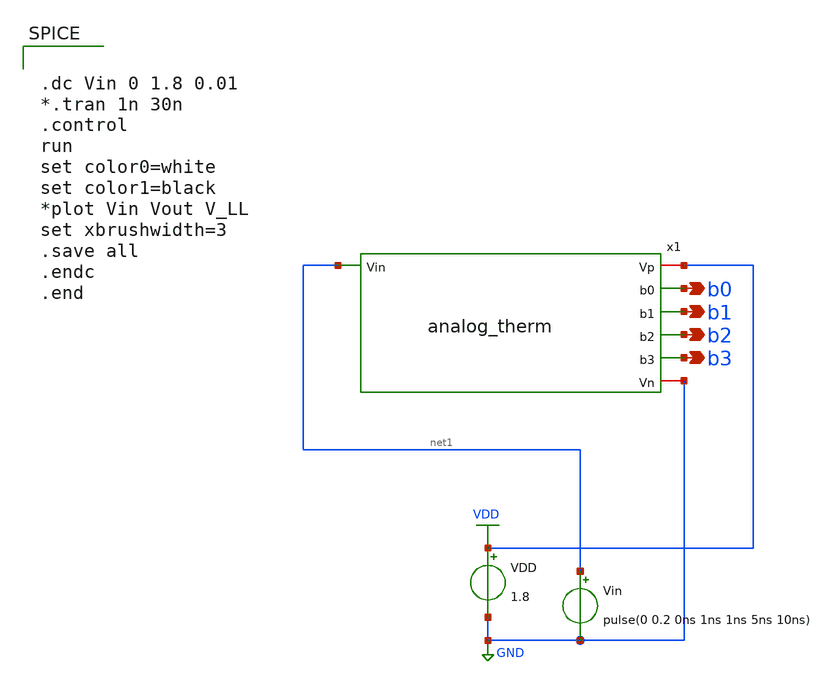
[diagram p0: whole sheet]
** sch_path: xschem/Vth_sch/Pre_layout/Analog_with_sub.sch
**.subckt Analog_with_sub b0 b1 b2 b3
*.opin b0
*.opin b1
*.opin b2
*.opin b3
VDD VDD GND 1.8
Vin net1 GND pulse(0 0.2 0ns 1ns 1ns 5ns 10ns)
x1 VDD net1 b0 b1 b2 b3 GND analog_therm
**** begin user architecture code


.lib /usr/local/share/pdk/sky130A/libs.tech/ngspice/sky130.lib.spice tt
.include /usr/local/share/pdk/sky130A/libs.ref/sky130_fd_sc_hd/spice/sky130_fd_sc_hd.spice
.save all





.dc Vin 0 1.8 0.01
*.tran 1n 30n
.control
run
set color0=white
set color1=black
*plot Vin Vout V_LL
set xbrushwidth=3
.save all
.endc
.end


**** end user architecture code
**.ends

* expanding   symbol:  analog_therm.sym # of pins=7
** sym_path: xschem/Vth_sch/Symbol/analog_therm.sym
** sch_path: xschem/Vth_sch/Symbol/analog_therm.sch
.subckt analog_therm Vp Vin b0 b1 b2 b3 Vn
*.opin b0
*.ipin Vin
*.opin b1
*.opin b2
*.opin b3
*.iopin Vp
*.iopin Vn
x1 p1 p0 VGND VNB VPB VPWR 2 sky130_fd_sc_hd__nand2_1
x2 p1 p0 p2 VGND VNB VPB VPWR 3 sky130_fd_sc_hd__nand3_1
x3 p1 p0 p3 p2 VGND VNB VPB VPWR 4 sky130_fd_sc_hd__nand4_1
x4 p5 p4 VGND VNB VPB VPWR 5 sky130_fd_sc_hd__nand2_1
x5 p5 p4 p7 p6 VGND VNB VPB VPWR 6 sky130_fd_sc_hd__nand4_1
x6 4 6 VGND VNB VPB VPWR 7 sky130_fd_sc_hd__nor2_1
x7 p8 p9 VGND VNB VPB VPWR 8 sky130_fd_sc_hd__nand2_1
x8 p11 p10 VGND VNB VPB VPWR 9 sky130_fd_sc_hd__nand2_1
x9 4 6 8 9 VGND VNB VPB VPWR 10 sky130_fd_sc_hd__nor4_1
x10 p13 p12 VGND VNB VPB VPWR 11 sky130_fd_sc_hd__and2_0
x11 10 11 VGND VNB VPB VPWR 12 sky130_fd_sc_hd__nand2_1
x12 p14 10 11 VGND VNB VPB VPWR 13 sky130_fd_sc_hd__nand3_1
x13 p7 5 VGND VNB VPB VPWR 14 sky130_fd_sc_hd__nor2_1
x14 p5 p7 p6 VGND VNB VPB VPWR 15 sky130_fd_sc_hd__nor3_1
x15 p6 14 15 p4 VGND VNB VPB VPWR 16 sky130_fd_sc_hd__a22oi_1
x16 p13 p14 VGND VNB VPB VPWR 17 sky130_fd_sc_hd__nor2_1
x17 p13 p12 p14 VGND VNB VPB VPWR 18 sky130_fd_sc_hd__or3_1
x18 p11 p10 VGND VNB VPB VPWR 19 sky130_fd_sc_hd__lpflow_inputiso1p_1
x19 p8 p9 18 19 VGND VNB VPB VPWR 20 sky130_fd_sc_hd__nor4_1
x20 4 20 VGND VNB VPB VPWR 21 sky130_fd_sc_hd__nand2b_1
x21 p9 18 19 p8 VGND VNB VPB VPWR 22 sky130_fd_sc_hd__nor4b_1
x22 p11 8 18 VGND VNB VPB VPWR 23 sky130_fd_sc_hd__nor3_1
x23 p11 1 8 18 VGND VNB VPB VPWR 24 sky130_fd_sc_hd__nor4_1
x24 22 24 7 VGND VNB VPB VPWR 25 sky130_fd_sc_hd__o21ai_0
x25 p1 p2 p0 VGND VNB VPB VPWR 26 sky130_fd_sc_hd__or3b_1
x26 p5 p4 p7 p6 VGND VNB VPB VPWR 27 sky130_fd_sc_hd__or4_1
x27 3 26 27 p3 VGND VNB VPB VPWR 28 sky130_fd_sc_hd__a211oi_1
x28 p12 10 17 20 28 VGND VNB VPB VPWR 29 sky130_fd_sc_hd__a32oi_1
x29 16 21 25 29 13 VGND VNB VPB VPWR b0 sky130_fd_sc_hd__o2111ai_1
x30 4 14 20 VGND VNB VPB VPWR 30 sky130_fd_sc_hd__nand3b_1
x31 7 23 VGND VNB VPB VPWR 31 sky130_fd_sc_hd__nand2_1
x32 p3 2 27 VGND VNB VPB VPWR 32 sky130_fd_sc_hd__nor3_1
x33 20 32 VGND VNB VPB VPWR 33 sky130_fd_sc_hd__nand2_1
x34 12 30 31 33 VGND VNB VPB VPWR b1 sky130_fd_sc_hd__nand4_1
x35 11 17 10 VGND VNB VPB VPWR 34 sky130_fd_sc_hd__o21ai_0
x36 14 15 VGND VNB VPB VPWR 35 sky130_fd_sc_hd__nor2_1
x37 21 35 34 VGND VNB VPB VPWR b2 sky130_fd_sc_hd__o21ai_0
x38 20 22 23 7 VGND VNB VPB VPWR 36 sky130_fd_sc_hd__o31ai_1
x39 34 36 VGND VNB VPB VPWR b3 sky130_fd_sc_hd__nand2_1
**** begin user architecture code


vvpwr vpwr 0 dc 1.8
vvgnd vgnd 0 dc 0


**** end user architecture code
x41 p10 VGND VNB VPB VPWR 1 sky130_fd_sc_hd__clkinv_1
x40 Vin Vp p0 p1 p2 p3 p4 p5 p6 p7 p8 p9 p10 p11 p12 p13 p14 Vn Analog
.ends


* expanding   symbol:  Analog.sym # of pins=18
** sym_path: xschem/Vth_sch/Symbol/Analog.sym
** sch_path: xschem/Vth_sch/Symbol/Analog.sch
.subckt Analog Vin Vp V1 V2 V3 V4 V5 V6 V7 V8 V9 V10 V11 V12 V13 V14 V15 Vn
*.ipin Vin
*.opin V1
*.opin V3
*.opin V5
*.opin V7
*.opin V9
*.opin V11
*.opin V13
*.opin V15
*.opin V2
*.opin V4
*.opin V6
*.opin V8
*.opin V10
*.opin V12
*.opin V14
*.iopin Vp
*.iopin Vn
x1 Vp Vin V1 Vn th01
x2 Vp Vin V2 Vn th02
x3 Vp V3 Vin Vn th03
x4 Vp V4 Vin Vn th04
x5 Vp V5 Vin Vn th05
x6 Vp Vin V6 Vn th06
x7 Vp Vin V7 Vn th07
x8 Vp Vin V8 Vn th08
x9 Vp V9 Vin Vn th09
x10 Vp V10 Vin Vn th10
x11 Vp V11 Vin Vn th11
x12 Vp V12 Vin Vn th12
x13 Vp V13 Vin Vn th13
x14 Vp V14 Vin Vn th14
x15 Vp V15 Vin Vn th15
.ends


* expanding   symbol:  Symbol/th01.sym # of pins=4
** sym_path: xschem/Vth_sch/Symbol/th01.sym
** sch_path: xschem/Vth_sch/Symbol/th01.sch
.subckt th01 Vp Vin V01 Vn
*.ipin Vin
*.opin V01
*.iopin Vp
*.iopin Vn
XM3 V01 net1 Vp Vp sky130_fd_pr__pfet_01v8 L=0.15 W=1.5 nf=1 ad='int((nf+1)/2) * W/nf * 0.29' as='int((nf+2)/2) * W/nf * 0.29'
+ pd='2*int((nf+1)/2) * (W/nf + 0.29)' ps='2*int((nf+2)/2) * (W/nf + 0.29)' nrd='0.29 / W' nrs='0.29 / W'
+ sa=0 sb=0 sd=0 mult=1 m=1
XM4 V01 net1 Vn Vn sky130_fd_pr__nfet_01v8 L=1.50 W=0.36 nf=1 ad='int((nf+1)/2) * W/nf * 0.29' as='int((nf+2)/2) * W/nf * 0.29'
+ pd='2*int((nf+1)/2) * (W/nf + 0.29)' ps='2*int((nf+2)/2) * (W/nf + 0.29)' nrd='0.29 / W' nrs='0.29 / W'
+ sa=0 sb=0 sd=0 mult=1 m=1
XM1 net1 Vin net2 Vp sky130_fd_pr__pfet_01v8 L=3.5 W=0.42 nf=1 ad='int((nf+1)/2) * W/nf * 0.29' as='int((nf+2)/2) * W/nf * 0.29'
+ pd='2*int((nf+1)/2) * (W/nf + 0.29)' ps='2*int((nf+2)/2) * (W/nf + 0.29)' nrd='0.29 / W' nrs='0.29 / W'
+ sa=0 sb=0 sd=0 mult=1 m=1
XM0 net1 Vin Vn Vn sky130_fd_pr__nfet_01v8 L=0.15 W=3.525 nf=1 ad='int((nf+1)/2) * W/nf * 0.29' as='int((nf+2)/2) * W/nf * 0.29'
+ pd='2*int((nf+1)/2) * (W/nf + 0.29)' ps='2*int((nf+2)/2) * (W/nf + 0.29)' nrd='0.29 / W' nrs='0.29 / W'
+ sa=0 sb=0 sd=0 mult=1 m=1
XM2 Vp Vp net2 Vn sky130_fd_pr__nfet_01v8 L=3.5 W=0.36 nf=1 ad='int((nf+1)/2) * W/nf * 0.29' as='int((nf+2)/2) * W/nf * 0.29'
+ pd='2*int((nf+1)/2) * (W/nf + 0.29)' ps='2*int((nf+2)/2) * (W/nf + 0.29)' nrd='0.29 / W' nrs='0.29 / W'
+ sa=0 sb=0 sd=0 mult=1 m=1
.ends


* expanding   symbol:  Symbol/th02.sym # of pins=4
** sym_path: xschem/Vth_sch/Symbol/th02.sym
** sch_path: xschem/Vth_sch/Symbol/th02.sch
.subckt th02 Vp Vin V02 Vn
*.ipin Vin
*.opin V02
*.iopin Vp
*.iopin Vn
XM3 V02 net1 Vp Vp sky130_fd_pr__pfet_01v8 L=0.15 W=1.5 nf=1 ad='int((nf+1)/2) * W/nf * 0.29' as='int((nf+2)/2) * W/nf * 0.29'
+ pd='2*int((nf+1)/2) * (W/nf + 0.29)' ps='2*int((nf+2)/2) * (W/nf + 0.29)' nrd='0.29 / W' nrs='0.29 / W'
+ sa=0 sb=0 sd=0 mult=1 m=1
XM4 V02 net1 Vn Vn sky130_fd_pr__nfet_01v8 L=1.50 W=0.36 nf=1 ad='int((nf+1)/2) * W/nf * 0.29' as='int((nf+2)/2) * W/nf * 0.29'
+ pd='2*int((nf+1)/2) * (W/nf + 0.29)' ps='2*int((nf+2)/2) * (W/nf + 0.29)' nrd='0.29 / W' nrs='0.29 / W'
+ sa=0 sb=0 sd=0 mult=1 m=1
XM1 net1 Vin net2 Vp sky130_fd_pr__pfet_01v8 L=1.53 W=0.42 nf=1 ad='int((nf+1)/2) * W/nf * 0.29' as='int((nf+2)/2) * W/nf * 0.29'
+ pd='2*int((nf+1)/2) * (W/nf + 0.29)' ps='2*int((nf+2)/2) * (W/nf + 0.29)' nrd='0.29 / W' nrs='0.29 / W'
+ sa=0 sb=0 sd=0 mult=1 m=1
XM0 net1 Vin Vn Vn sky130_fd_pr__nfet_01v8 L=0.15 W=1.5 nf=2 ad='int((nf+1)/2) * W/nf * 0.29' as='int((nf+2)/2) * W/nf * 0.29'
+ pd='2*int((nf+1)/2) * (W/nf + 0.29)' ps='2*int((nf+2)/2) * (W/nf + 0.29)' nrd='0.29 / W' nrs='0.29 / W'
+ sa=0 sb=0 sd=0 mult=1 m=1
XM2 Vp Vp net2 Vn sky130_fd_pr__nfet_01v8 L=1.54 W=0.36 nf=1 ad='int((nf+1)/2) * W/nf * 0.29' as='int((nf+2)/2) * W/nf * 0.29'
+ pd='2*int((nf+1)/2) * (W/nf + 0.29)' ps='2*int((nf+2)/2) * (W/nf + 0.29)' nrd='0.29 / W' nrs='0.29 / W'
+ sa=0 sb=0 sd=0 mult=1 m=1
.ends


* expanding   symbol:  Symbol/th03.sym # of pins=4
** sym_path: xschem/Vth_sch/Symbol/th03.sym
** sch_path: xschem/Vth_sch/Symbol/th03.sch
.subckt th03 Vp V03 Vin Vn
*.opin Vn
*.opin Vp
*.ipin Vin
*.opin V03
XM3 V03 net1 Vp Vp sky130_fd_pr__pfet_01v8 L=0.156 W=1.0 nf=1 ad='int((nf+1)/2) * W/nf * 0.29' as='int((nf+2)/2) * W/nf * 0.29'
+ pd='2*int((nf+1)/2) * (W/nf + 0.29)' ps='2*int((nf+2)/2) * (W/nf + 0.29)' nrd='0.29 / W' nrs='0.29 / W'
+ sa=0 sb=0 sd=0 mult=1 m=1
XM4 V03 net1 Vn Vn sky130_fd_pr__nfet_01v8 L=1.5 W=0.40 nf=1 ad='int((nf+1)/2) * W/nf * 0.29' as='int((nf+2)/2) * W/nf * 0.29'
+ pd='2*int((nf+1)/2) * (W/nf + 0.29)' ps='2*int((nf+2)/2) * (W/nf + 0.29)' nrd='0.29 / W' nrs='0.29 / W'
+ sa=0 sb=0 sd=0 mult=1 m=1
XM1 net1 Vin net2 Vp sky130_fd_pr__pfet_01v8 L=1.36 W=0.44 nf=1 ad='int((nf+1)/2) * W/nf * 0.29' as='int((nf+2)/2) * W/nf * 0.29'
+ pd='2*int((nf+1)/2) * (W/nf + 0.29)' ps='2*int((nf+2)/2) * (W/nf + 0.29)' nrd='0.29 / W' nrs='0.29 / W'
+ sa=0 sb=0 sd=0 mult=1 m=1
XM0 net1 Vin Vn Vn sky130_fd_pr__nfet_01v8 L=0.153 W=1.1 nf=1 ad='int((nf+1)/2) * W/nf * 0.29' as='int((nf+2)/2) * W/nf * 0.29'
+ pd='2*int((nf+1)/2) * (W/nf + 0.29)' ps='2*int((nf+2)/2) * (W/nf + 0.29)' nrd='0.29 / W' nrs='0.29 / W'
+ sa=0 sb=0 sd=0 mult=1 m=1
XM2 Vp Vp net2 Vn sky130_fd_pr__nfet_01v8 L=1.5 W=0.36 nf=1 ad='int((nf+1)/2) * W/nf * 0.29' as='int((nf+2)/2) * W/nf * 0.29'
+ pd='2*int((nf+1)/2) * (W/nf + 0.29)' ps='2*int((nf+2)/2) * (W/nf + 0.29)' nrd='0.29 / W' nrs='0.29 / W'
+ sa=0 sb=0 sd=0 mult=1 m=1
.ends


* expanding   symbol:  Symbol/th04.sym # of pins=4
** sym_path: xschem/Vth_sch/Symbol/th04.sym
** sch_path: xschem/Vth_sch/Symbol/th04.sch
.subckt th04 Vp V04 Vin Vn
*.opin Vn
*.opin Vp
*.ipin Vin
*.opin V04
XM3 V04 net1 Vp Vp sky130_fd_pr__pfet_01v8 L=0.220 W=0.42 nf=1 ad='int((nf+1)/2) * W/nf * 0.29' as='int((nf+2)/2) * W/nf * 0.29'
+ pd='2*int((nf+1)/2) * (W/nf + 0.29)' ps='2*int((nf+2)/2) * (W/nf + 0.29)' nrd='0.29 / W' nrs='0.29 / W'
+ sa=0 sb=0 sd=0 mult=1 m=1
XM4 V04 net1 Vn Vn sky130_fd_pr__nfet_01v8 L=0.193 W=0.36 nf=1 ad='int((nf+1)/2) * W/nf * 0.29' as='int((nf+2)/2) * W/nf * 0.29'
+ pd='2*int((nf+1)/2) * (W/nf + 0.29)' ps='2*int((nf+2)/2) * (W/nf + 0.29)' nrd='0.29 / W' nrs='0.29 / W'
+ sa=0 sb=0 sd=0 mult=1 m=1
XM1 net1 Vin net2 Vp sky130_fd_pr__pfet_01v8 L=0.193 W=0.42 nf=1 ad='int((nf+1)/2) * W/nf * 0.29' as='int((nf+2)/2) * W/nf * 0.29'
+ pd='2*int((nf+1)/2) * (W/nf + 0.29)' ps='2*int((nf+2)/2) * (W/nf + 0.29)' nrd='0.29 / W' nrs='0.29 / W'
+ sa=0 sb=0 sd=0 mult=1 m=1
XM0 net1 Vin Vn Vn sky130_fd_pr__nfet_01v8 L=0.220 W=0.36 nf=1 ad='int((nf+1)/2) * W/nf * 0.29' as='int((nf+2)/2) * W/nf * 0.29'
+ pd='2*int((nf+1)/2) * (W/nf + 0.29)' ps='2*int((nf+2)/2) * (W/nf + 0.29)' nrd='0.29 / W' nrs='0.29 / W'
+ sa=0 sb=0 sd=0 mult=1 m=1
XM2 Vp Vp net2 Vn sky130_fd_pr__nfet_01v8 L=0.151 W=0.36 nf=1 ad='int((nf+1)/2) * W/nf * 0.29' as='int((nf+2)/2) * W/nf * 0.29'
+ pd='2*int((nf+1)/2) * (W/nf + 0.29)' ps='2*int((nf+2)/2) * (W/nf + 0.29)' nrd='0.29 / W' nrs='0.29 / W'
+ sa=0 sb=0 sd=0 mult=1 m=1
.ends


* expanding   symbol:  Symbol/th05.sym # of pins=4
** sym_path: xschem/Vth_sch/Symbol/th05.sym
** sch_path: xschem/Vth_sch/Symbol/th05.sch
.subckt th05 Vp V05 Vin Vn
*.opin Vn
*.opin Vp
*.ipin Vin
*.opin V05
XM2 V05 net1 Vp Vp sky130_fd_pr__pfet_01v8 L=1.12 W=0.5 nf=1 ad='int((nf+1)/2) * W/nf * 0.29' as='int((nf+2)/2) * W/nf * 0.29'
+ pd='2*int((nf+1)/2) * (W/nf + 0.29)' ps='2*int((nf+2)/2) * (W/nf + 0.29)' nrd='0.29 / W' nrs='0.29 / W'
+ sa=0 sb=0 sd=0 mult=1 m=1
XM3 V05 net1 Vn Vn sky130_fd_pr__nfet_01v8 L=0.18 W=1.0 nf=1 ad='int((nf+1)/2) * W/nf * 0.29' as='int((nf+2)/2) * W/nf * 0.29'
+ pd='2*int((nf+1)/2) * (W/nf + 0.29)' ps='2*int((nf+2)/2) * (W/nf + 0.29)' nrd='0.29 / W' nrs='0.29 / W'
+ sa=0 sb=0 sd=0 mult=1 m=1
XM1 net1 Vin Vp Vp sky130_fd_pr__pfet_01v8 L=1.633 W=0.42 nf=1 ad='int((nf+1)/2) * W/nf * 0.29' as='int((nf+2)/2) * W/nf * 0.29'
+ pd='2*int((nf+1)/2) * (W/nf + 0.29)' ps='2*int((nf+2)/2) * (W/nf + 0.29)' nrd='0.29 / W' nrs='0.29 / W'
+ sa=0 sb=0 sd=0 mult=1 m=1
XM0 net1 Vin Vn Vn sky130_fd_pr__nfet_01v8 L=0.2 W=2.00 nf=1 ad='int((nf+1)/2) * W/nf * 0.29' as='int((nf+2)/2) * W/nf * 0.29'
+ pd='2*int((nf+1)/2) * (W/nf + 0.29)' ps='2*int((nf+2)/2) * (W/nf + 0.29)' nrd='0.29 / W' nrs='0.29 / W'
+ sa=0 sb=0 sd=0 mult=1 m=1
.ends


* expanding   symbol:  Symbol/th06.sym # of pins=4
** sym_path: xschem/Vth_sch/Symbol/th06.sym
** sch_path: xschem/Vth_sch/Symbol/th06.sch
.subckt th06 Vp Vin V06 Vn
*.opin Vn
*.opin Vp
*.ipin Vin
*.opin V06
XM2 V06 net1 Vp Vp sky130_fd_pr__pfet_01v8 L=0.436 W=0.422 nf=1 ad='int((nf+1)/2) * W/nf * 0.29' as='int((nf+2)/2) * W/nf * 0.29'
+ pd='2*int((nf+1)/2) * (W/nf + 0.29)' ps='2*int((nf+2)/2) * (W/nf + 0.29)' nrd='0.29 / W' nrs='0.29 / W'
+ sa=0 sb=0 sd=0 mult=1 m=1
XM3 V06 net1 Vn Vn sky130_fd_pr__nfet_01v8 L=0.15 W=0.462 nf=1 ad='int((nf+1)/2) * W/nf * 0.29' as='int((nf+2)/2) * W/nf * 0.29'
+ pd='2*int((nf+1)/2) * (W/nf + 0.29)' ps='2*int((nf+2)/2) * (W/nf + 0.29)' nrd='0.29 / W' nrs='0.29 / W'
+ sa=0 sb=0 sd=0 mult=1 m=1
XM1 net1 Vin Vp Vp sky130_fd_pr__pfet_01v8 L=0.494 W=0.42 nf=1 ad='int((nf+1)/2) * W/nf * 0.29' as='int((nf+2)/2) * W/nf * 0.29'
+ pd='2*int((nf+1)/2) * (W/nf + 0.29)' ps='2*int((nf+2)/2) * (W/nf + 0.29)' nrd='0.29 / W' nrs='0.29 / W'
+ sa=0 sb=0 sd=0 mult=1 m=1
XM0 net1 Vin Vn Vn sky130_fd_pr__nfet_01v8 L=0.152 W=0.393 nf=1 ad='int((nf+1)/2) * W/nf * 0.29' as='int((nf+2)/2) * W/nf * 0.29'
+ pd='2*int((nf+1)/2) * (W/nf + 0.29)' ps='2*int((nf+2)/2) * (W/nf + 0.29)' nrd='0.29 / W' nrs='0.29 / W'
+ sa=0 sb=0 sd=0 mult=1 m=1
.ends


* expanding   symbol:  Symbol/th07.sym # of pins=4
** sym_path: xschem/Vth_sch/Symbol/th07.sym
** sch_path: xschem/Vth_sch/Symbol/th07.sch
.subckt th07 Vp Vin V07 Vn
*.opin Vn
*.opin Vp
*.ipin Vin
*.opin V07
XM2 V07 net1 Vp Vp sky130_fd_pr__pfet_01v8 L=0.5 W=0.42 nf=1 ad='int((nf+1)/2) * W/nf * 0.29' as='int((nf+2)/2) * W/nf * 0.29'
+ pd='2*int((nf+1)/2) * (W/nf + 0.29)' ps='2*int((nf+2)/2) * (W/nf + 0.29)' nrd='0.29 / W' nrs='0.29 / W'
+ sa=0 sb=0 sd=0 mult=1 m=1
XM3 V07 net1 Vn Vn sky130_fd_pr__nfet_01v8 L=0.15 W=0.462 nf=1 ad='int((nf+1)/2) * W/nf * 0.29' as='int((nf+2)/2) * W/nf * 0.29'
+ pd='2*int((nf+1)/2) * (W/nf + 0.29)' ps='2*int((nf+2)/2) * (W/nf + 0.29)' nrd='0.29 / W' nrs='0.29 / W'
+ sa=0 sb=0 sd=0 mult=1 m=1
XM1 net1 Vin Vp Vp sky130_fd_pr__pfet_01v8 L=0.151 W=0.42 nf=1 ad='int((nf+1)/2) * W/nf * 0.29' as='int((nf+2)/2) * W/nf * 0.29'
+ pd='2*int((nf+1)/2) * (W/nf + 0.29)' ps='2*int((nf+2)/2) * (W/nf + 0.29)' nrd='0.29 / W' nrs='0.29 / W'
+ sa=0 sb=0 sd=0 mult=1 m=1
XM0 net1 Vin Vn Vn sky130_fd_pr__nfet_01v8 L=0.155 W=0.36 nf=1 ad='int((nf+1)/2) * W/nf * 0.29' as='int((nf+2)/2) * W/nf * 0.29'
+ pd='2*int((nf+1)/2) * (W/nf + 0.29)' ps='2*int((nf+2)/2) * (W/nf + 0.29)' nrd='0.29 / W' nrs='0.29 / W'
+ sa=0 sb=0 sd=0 mult=1 m=1
.ends


* expanding   symbol:  Symbol/th08.sym # of pins=4
** sym_path: xschem/Vth_sch/Symbol/th08.sym
** sch_path: xschem/Vth_sch/Symbol/th08.sch
.subckt th08 Vp Vin V08 Vn
*.opin Vn
*.opin Vp
*.ipin Vin
*.opin V08
XM2 V08 net1 Vp Vp sky130_fd_pr__pfet_01v8 L=0.48 W=0.43 nf=1 ad='int((nf+1)/2) * W/nf * 0.29' as='int((nf+2)/2) * W/nf * 0.29'
+ pd='2*int((nf+1)/2) * (W/nf + 0.29)' ps='2*int((nf+2)/2) * (W/nf + 0.29)' nrd='0.29 / W' nrs='0.29 / W'
+ sa=0 sb=0 sd=0 mult=1 m=1
XM3 V08 net1 Vn Vn sky130_fd_pr__nfet_01v8 L=0.15 W=0.468 nf=1 ad='int((nf+1)/2) * W/nf * 0.29' as='int((nf+2)/2) * W/nf * 0.29'
+ pd='2*int((nf+1)/2) * (W/nf + 0.29)' ps='2*int((nf+2)/2) * (W/nf + 0.29)' nrd='0.29 / W' nrs='0.29 / W'
+ sa=0 sb=0 sd=0 mult=1 m=1
XM1 net1 Vin Vp Vp sky130_fd_pr__pfet_01v8 L=0.16 W=0.668 nf=1 ad='int((nf+1)/2) * W/nf * 0.29' as='int((nf+2)/2) * W/nf * 0.29'
+ pd='2*int((nf+1)/2) * (W/nf + 0.29)' ps='2*int((nf+2)/2) * (W/nf + 0.29)' nrd='0.29 / W' nrs='0.29 / W'
+ sa=0 sb=0 sd=0 mult=1 m=1
XM0 net1 Vin Vn Vn sky130_fd_pr__nfet_01v8 L=1.13 W=0.36 nf=1 ad='int((nf+1)/2) * W/nf * 0.29' as='int((nf+2)/2) * W/nf * 0.29'
+ pd='2*int((nf+1)/2) * (W/nf + 0.29)' ps='2*int((nf+2)/2) * (W/nf + 0.29)' nrd='0.29 / W' nrs='0.29 / W'
+ sa=0 sb=0 sd=0 mult=1 m=1
.ends


* expanding   symbol:  Symbol/th09.sym # of pins=4
** sym_path: xschem/Vth_sch/Symbol/th09.sym
** sch_path: xschem/Vth_sch/Symbol/th09.sch
.subckt th09 Vp V09 Vin Vn
*.ipin Vin
*.opin V09
*.opin Vn
*.opin Vp
XM2 net2 net1 Vp Vp sky130_fd_pr__pfet_01v8 L=1.57 W=0.42 nf=1 ad='int((nf+1)/2) * W/nf * 0.29' as='int((nf+2)/2) * W/nf * 0.29'
+ pd='2*int((nf+1)/2) * (W/nf + 0.29)' ps='2*int((nf+2)/2) * (W/nf + 0.29)' nrd='0.29 / W' nrs='0.29 / W'
+ sa=0 sb=0 sd=0 mult=1 m=1
XM3 V09 net1 net2 Vp sky130_fd_pr__pfet_01v8 L=1.57 W=0.42 nf=1 ad='int((nf+1)/2) * W/nf * 0.29' as='int((nf+2)/2) * W/nf * 0.29'
+ pd='2*int((nf+1)/2) * (W/nf + 0.29)' ps='2*int((nf+2)/2) * (W/nf + 0.29)' nrd='0.29 / W' nrs='0.29 / W'
+ sa=0 sb=0 sd=0 mult=1 m=1
XM4 V09 net1 Vn Vn sky130_fd_pr__nfet_01v8 L=0.15 W=1.57 nf=1 ad='int((nf+1)/2) * W/nf * 0.29' as='int((nf+2)/2) * W/nf * 0.29'
+ pd='2*int((nf+1)/2) * (W/nf + 0.29)' ps='2*int((nf+2)/2) * (W/nf + 0.29)' nrd='0.29 / W' nrs='0.29 / W'
+ sa=0 sb=0 sd=0 mult=1 m=1
XM1 net1 Vin Vp Vp sky130_fd_pr__pfet_01v8 L=0.15 W=1.58 nf=1 ad='int((nf+1)/2) * W/nf * 0.29' as='int((nf+2)/2) * W/nf * 0.29'
+ pd='2*int((nf+1)/2) * (W/nf + 0.29)' ps='2*int((nf+2)/2) * (W/nf + 0.29)' nrd='0.29 / W' nrs='0.29 / W'
+ sa=0 sb=0 sd=0 mult=1 m=1
XM0 net1 Vin Vn Vn sky130_fd_pr__nfet_01v8 L=1.58 W=0.36 nf=1 ad='int((nf+1)/2) * W/nf * 0.29' as='int((nf+2)/2) * W/nf * 0.29'
+ pd='2*int((nf+1)/2) * (W/nf + 0.29)' ps='2*int((nf+2)/2) * (W/nf + 0.29)' nrd='0.29 / W' nrs='0.29 / W'
+ sa=0 sb=0 sd=0 mult=1 m=1
.ends


* expanding   symbol:  Symbol/th10.sym # of pins=4
** sym_path: xschem/Vth_sch/Symbol/th10.sym
** sch_path: xschem/Vth_sch/Symbol/th10.sch
.subckt th10 Vp V10 Vin Vn
*.opin Vn
*.opin Vp
*.ipin Vin
*.opin V10
XM3 V10 net1 Vp Vp sky130_fd_pr__pfet_01v8 L=0.15 W=0.42 nf=1 ad='int((nf+1)/2) * W/nf * 0.29' as='int((nf+2)/2) * W/nf * 0.29'
+ pd='2*int((nf+1)/2) * (W/nf + 0.29)' ps='2*int((nf+2)/2) * (W/nf + 0.29)' nrd='0.29 / W' nrs='0.29 / W'
+ sa=0 sb=0 sd=0 mult=1 m=1
XM4 V10 net1 Vn Vn sky130_fd_pr__nfet_01v8 L=0.18 W=0.42 nf=1 ad='int((nf+1)/2) * W/nf * 0.29' as='int((nf+2)/2) * W/nf * 0.29'
+ pd='2*int((nf+1)/2) * (W/nf + 0.29)' ps='2*int((nf+2)/2) * (W/nf + 0.29)' nrd='0.29 / W' nrs='0.29 / W'
+ sa=0 sb=0 sd=0 mult=1 m=1
XM2 net1 Vin Vp Vp sky130_fd_pr__pfet_01v8 L=0.28 W=0.42 nf=1 ad='int((nf+1)/2) * W/nf * 0.29' as='int((nf+2)/2) * W/nf * 0.29'
+ pd='2*int((nf+1)/2) * (W/nf + 0.29)' ps='2*int((nf+2)/2) * (W/nf + 0.29)' nrd='0.29 / W' nrs='0.29 / W'
+ sa=0 sb=0 sd=0 mult=1 m=1
XM1 net1 Vin net2 Vn sky130_fd_pr__nfet_01v8 L=0.46 W=0.40 nf=1 ad='int((nf+1)/2) * W/nf * 0.29' as='int((nf+2)/2) * W/nf * 0.29'
+ pd='2*int((nf+1)/2) * (W/nf + 0.29)' ps='2*int((nf+2)/2) * (W/nf + 0.29)' nrd='0.29 / W' nrs='0.29 / W'
+ sa=0 sb=0 sd=0 mult=1 m=1
XM0 Vn Vn net2 Vp sky130_fd_pr__pfet_01v8 L=0.15 W=1 nf=1 ad='int((nf+1)/2) * W/nf * 0.29' as='int((nf+2)/2) * W/nf * 0.29'
+ pd='2*int((nf+1)/2) * (W/nf + 0.29)' ps='2*int((nf+2)/2) * (W/nf + 0.29)' nrd='0.29 / W' nrs='0.29 / W'
+ sa=0 sb=0 sd=0 mult=1 m=1
.ends


* expanding   symbol:  Symbol/th11.sym # of pins=4
** sym_path: xschem/Vth_sch/Symbol/th11.sym
** sch_path: xschem/Vth_sch/Symbol/th11.sch
.subckt th11 Vp V11 Vin Vn
*.opin Vn
*.opin Vp
*.ipin Vin
*.opin V11
XM3 V11 net1 Vp Vp sky130_fd_pr__pfet_01v8 L=0.5 W=0.42 nf=1 ad='int((nf+1)/2) * W/nf * 0.29' as='int((nf+2)/2) * W/nf * 0.29'
+ pd='2*int((nf+1)/2) * (W/nf + 0.29)' ps='2*int((nf+2)/2) * (W/nf + 0.29)' nrd='0.29 / W' nrs='0.29 / W'
+ sa=0 sb=0 sd=0 mult=1 m=1
XM4 V11 net1 Vn Vn sky130_fd_pr__nfet_01v8 L=0.15 W=0.5 nf=1 ad='int((nf+1)/2) * W/nf * 0.29' as='int((nf+2)/2) * W/nf * 0.29'
+ pd='2*int((nf+1)/2) * (W/nf + 0.29)' ps='2*int((nf+2)/2) * (W/nf + 0.29)' nrd='0.29 / W' nrs='0.29 / W'
+ sa=0 sb=0 sd=0 mult=1 m=1
XM2 net1 Vin Vp Vp sky130_fd_pr__pfet_01v8 L=0.15 W=0.43 nf=1 ad='int((nf+1)/2) * W/nf * 0.29' as='int((nf+2)/2) * W/nf * 0.29'
+ pd='2*int((nf+1)/2) * (W/nf + 0.29)' ps='2*int((nf+2)/2) * (W/nf + 0.29)' nrd='0.29 / W' nrs='0.29 / W'
+ sa=0 sb=0 sd=0 mult=1 m=1
XM1 net1 Vin net2 Vn sky130_fd_pr__nfet_01v8 L=1.8 W=0.36 nf=1 ad='int((nf+1)/2) * W/nf * 0.29' as='int((nf+2)/2) * W/nf * 0.29'
+ pd='2*int((nf+1)/2) * (W/nf + 0.29)' ps='2*int((nf+2)/2) * (W/nf + 0.29)' nrd='0.29 / W' nrs='0.29 / W'
+ sa=0 sb=0 sd=0 mult=1 m=1
XM0 Vn Vn net2 Vp sky130_fd_pr__pfet_01v8 L=0.15 W=2 nf=1 ad='int((nf+1)/2) * W/nf * 0.29' as='int((nf+2)/2) * W/nf * 0.29'
+ pd='2*int((nf+1)/2) * (W/nf + 0.29)' ps='2*int((nf+2)/2) * (W/nf + 0.29)' nrd='0.29 / W' nrs='0.29 / W'
+ sa=0 sb=0 sd=0 mult=1 m=1
.ends


* expanding   symbol:  Symbol/th12.sym # of pins=4
** sym_path: xschem/Vth_sch/Symbol/th12.sym
** sch_path: xschem/Vth_sch/Symbol/th12.sch
.subckt th12 Vp V12 Vin Vn
*.opin Vn
*.opin Vp
*.ipin Vin
*.opin V12
XM3 V12 net1 Vp Vp sky130_fd_pr__pfet_01v8 L=1.0 W=0.42 nf=1 ad='int((nf+1)/2) * W/nf * 0.29' as='int((nf+2)/2) * W/nf * 0.29'
+ pd='2*int((nf+1)/2) * (W/nf + 0.29)' ps='2*int((nf+2)/2) * (W/nf + 0.29)' nrd='0.29 / W' nrs='0.29 / W'
+ sa=0 sb=0 sd=0 mult=1 m=1
XM4 V12 net1 Vn Vn sky130_fd_pr__nfet_01v8 L=0.15 W=1.0 nf=1 ad='int((nf+1)/2) * W/nf * 0.29' as='int((nf+2)/2) * W/nf * 0.29'
+ pd='2*int((nf+1)/2) * (W/nf + 0.29)' ps='2*int((nf+2)/2) * (W/nf + 0.29)' nrd='0.29 / W' nrs='0.29 / W'
+ sa=0 sb=0 sd=0 mult=1 m=1
XM2 net1 Vin Vp Vp sky130_fd_pr__pfet_01v8 L=0.15 W=1.0 nf=1 ad='int((nf+1)/2) * W/nf * 0.29' as='int((nf+2)/2) * W/nf * 0.29'
+ pd='2*int((nf+1)/2) * (W/nf + 0.29)' ps='2*int((nf+2)/2) * (W/nf + 0.29)' nrd='0.29 / W' nrs='0.29 / W'
+ sa=0 sb=0 sd=0 mult=1 m=1
XM1 net1 Vin net2 Vn sky130_fd_pr__nfet_01v8 L=2.90 W=0.36 nf=1 ad='int((nf+1)/2) * W/nf * 0.29' as='int((nf+2)/2) * W/nf * 0.29'
+ pd='2*int((nf+1)/2) * (W/nf + 0.29)' ps='2*int((nf+2)/2) * (W/nf + 0.29)' nrd='0.29 / W' nrs='0.29 / W'
+ sa=0 sb=0 sd=0 mult=1 m=1
XM0 Vn Vn net2 Vp sky130_fd_pr__pfet_01v8 L=0.151 W=1.349 nf=1 ad='int((nf+1)/2) * W/nf * 0.29' as='int((nf+2)/2) * W/nf * 0.29'
+ pd='2*int((nf+1)/2) * (W/nf + 0.29)' ps='2*int((nf+2)/2) * (W/nf + 0.29)' nrd='0.29 / W' nrs='0.29 / W'
+ sa=0 sb=0 sd=0 mult=1 m=1
.ends


* expanding   symbol:  Symbol/th13.sym # of pins=4
** sym_path: xschem/Vth_sch/Symbol/th13.sym
** sch_path: xschem/Vth_sch/Symbol/th13.sch
.subckt th13 Vp V13 Vin Vn
*.opin Vn
*.opin Vp
*.ipin Vin
*.opin V13
XM3 V13 net1 Vp Vp sky130_fd_pr__pfet_01v8 L=2 W=0.42 nf=1 ad='int((nf+1)/2) * W/nf * 0.29' as='int((nf+2)/2) * W/nf * 0.29'
+ pd='2*int((nf+1)/2) * (W/nf + 0.29)' ps='2*int((nf+2)/2) * (W/nf + 0.29)' nrd='0.29 / W' nrs='0.29 / W'
+ sa=0 sb=0 sd=0 mult=1 m=1
XM4 V13 net1 Vn Vn sky130_fd_pr__nfet_01v8 L=0.15 W=2 nf=1 ad='int((nf+1)/2) * W/nf * 0.29' as='int((nf+2)/2) * W/nf * 0.29'
+ pd='2*int((nf+1)/2) * (W/nf + 0.29)' ps='2*int((nf+2)/2) * (W/nf + 0.29)' nrd='0.29 / W' nrs='0.29 / W'
+ sa=0 sb=0 sd=0 mult=1 m=1
XM2 net1 Vin Vp Vp sky130_fd_pr__pfet_01v8 L=0.15 W=2.4 nf=1 ad='int((nf+1)/2) * W/nf * 0.29' as='int((nf+2)/2) * W/nf * 0.29'
+ pd='2*int((nf+1)/2) * (W/nf + 0.29)' ps='2*int((nf+2)/2) * (W/nf + 0.29)' nrd='0.29 / W' nrs='0.29 / W'
+ sa=0 sb=0 sd=0 mult=1 m=1
XM1 net1 Vin net2 Vn sky130_fd_pr__nfet_01v8 L=2.5 W=0.36 nf=1 ad='int((nf+1)/2) * W/nf * 0.29' as='int((nf+2)/2) * W/nf * 0.29'
+ pd='2*int((nf+1)/2) * (W/nf + 0.29)' ps='2*int((nf+2)/2) * (W/nf + 0.29)' nrd='0.29 / W' nrs='0.29 / W'
+ sa=0 sb=0 sd=0 mult=1 m=1
XM0 Vn Vn net2 Vp sky130_fd_pr__pfet_01v8 L=0.15 W=1 nf=1 ad='int((nf+1)/2) * W/nf * 0.29' as='int((nf+2)/2) * W/nf * 0.29'
+ pd='2*int((nf+1)/2) * (W/nf + 0.29)' ps='2*int((nf+2)/2) * (W/nf + 0.29)' nrd='0.29 / W' nrs='0.29 / W'
+ sa=0 sb=0 sd=0 mult=1 m=1
.ends


* expanding   symbol:  Symbol/th14.sym # of pins=4
** sym_path: xschem/Vth_sch/Symbol/th14.sym
** sch_path: xschem/Vth_sch/Symbol/th14.sch
.subckt th14 Vp V14 Vin Vn
*.opin Vn
*.opin Vp
*.ipin Vin
*.opin V14
XM3 V14 net1 Vp Vp sky130_fd_pr__pfet_01v8 L=3.3 W=0.42 nf=1 ad='int((nf+1)/2) * W/nf * 0.29' as='int((nf+2)/2) * W/nf * 0.29'
+ pd='2*int((nf+1)/2) * (W/nf + 0.29)' ps='2*int((nf+2)/2) * (W/nf + 0.29)' nrd='0.29 / W' nrs='0.29 / W'
+ sa=0 sb=0 sd=0 mult=1 m=1
XM4 V14 net1 Vn Vn sky130_fd_pr__nfet_01v8 L=0.15 W=2.5 nf=1 ad='int((nf+1)/2) * W/nf * 0.29' as='int((nf+2)/2) * W/nf * 0.29'
+ pd='2*int((nf+1)/2) * (W/nf + 0.29)' ps='2*int((nf+2)/2) * (W/nf + 0.29)' nrd='0.29 / W' nrs='0.29 / W'
+ sa=0 sb=0 sd=0 mult=1 m=1
XM2 net1 Vin Vp Vp sky130_fd_pr__pfet_01v8 L=0.8 W=0.5 nf=1 ad='int((nf+1)/2) * W/nf * 0.29' as='int((nf+2)/2) * W/nf * 0.29'
+ pd='2*int((nf+1)/2) * (W/nf + 0.29)' ps='2*int((nf+2)/2) * (W/nf + 0.29)' nrd='0.29 / W' nrs='0.29 / W'
+ sa=0 sb=0 sd=0 mult=1 m=1
XM1 net1 Vin net2 Vn sky130_fd_pr__nfet_01v8 L=1.55 W=0.36 nf=1 ad='int((nf+1)/2) * W/nf * 0.29' as='int((nf+2)/2) * W/nf * 0.29'
+ pd='2*int((nf+1)/2) * (W/nf + 0.29)' ps='2*int((nf+2)/2) * (W/nf + 0.29)' nrd='0.29 / W' nrs='0.29 / W'
+ sa=0 sb=0 sd=0 mult=1 m=1
XM0 Vn Vn net2 Vp sky130_fd_pr__pfet_01v8 L=0.227 W=0.5 nf=1 ad='int((nf+1)/2) * W/nf * 0.29' as='int((nf+2)/2) * W/nf * 0.29'
+ pd='2*int((nf+1)/2) * (W/nf + 0.29)' ps='2*int((nf+2)/2) * (W/nf + 0.29)' nrd='0.29 / W' nrs='0.29 / W'
+ sa=0 sb=0 sd=0 mult=1 m=1
.ends


* expanding   symbol:  Symbol/th15.sym # of pins=4
** sym_path: xschem/Vth_sch/Symbol/th15.sym
** sch_path: xschem/Vth_sch/Symbol/th15.sch
.subckt th15 Vp V15 Vin Vn
*.opin Vn
*.opin Vp
*.ipin Vin
*.opin V15
XM3 V15 net1 Vp Vp sky130_fd_pr__pfet_01v8 L=3.3 W=0.421 nf=1 ad='int((nf+1)/2) * W/nf * 0.29' as='int((nf+2)/2) * W/nf * 0.29'
+ pd='2*int((nf+1)/2) * (W/nf + 0.29)' ps='2*int((nf+2)/2) * (W/nf + 0.29)' nrd='0.29 / W' nrs='0.29 / W'
+ sa=0 sb=0 sd=0 mult=1 m=1
XM4 V15 net1 Vn Vn sky130_fd_pr__nfet_01v8 L=0.15 W=2.51 nf=1 ad='int((nf+1)/2) * W/nf * 0.29' as='int((nf+2)/2) * W/nf * 0.29'
+ pd='2*int((nf+1)/2) * (W/nf + 0.29)' ps='2*int((nf+2)/2) * (W/nf + 0.29)' nrd='0.29 / W' nrs='0.29 / W'
+ sa=0 sb=0 sd=0 mult=1 m=1
XM2 net1 Vin Vp Vp sky130_fd_pr__pfet_01v8 L=0.79 W=0.51 nf=1 ad='int((nf+1)/2) * W/nf * 0.29' as='int((nf+2)/2) * W/nf * 0.29'
+ pd='2*int((nf+1)/2) * (W/nf + 0.29)' ps='2*int((nf+2)/2) * (W/nf + 0.29)' nrd='0.29 / W' nrs='0.29 / W'
+ sa=0 sb=0 sd=0 mult=1 m=1
XM1 net1 Vin net2 Vn sky130_fd_pr__nfet_01v8 L=2.0 W=0.36 nf=1 ad='int((nf+1)/2) * W/nf * 0.29' as='int((nf+2)/2) * W/nf * 0.29'
+ pd='2*int((nf+1)/2) * (W/nf + 0.29)' ps='2*int((nf+2)/2) * (W/nf + 0.29)' nrd='0.29 / W' nrs='0.29 / W'
+ sa=0 sb=0 sd=0 mult=1 m=1
XM0 Vn Vn net2 Vp sky130_fd_pr__pfet_01v8 L=0.285 W=0.5 nf=1 ad='int((nf+1)/2) * W/nf * 0.29' as='int((nf+2)/2) * W/nf * 0.29'
+ pd='2*int((nf+1)/2) * (W/nf + 0.29)' ps='2*int((nf+2)/2) * (W/nf + 0.29)' nrd='0.29 / W' nrs='0.29 / W'
+ sa=0 sb=0 sd=0 mult=1 m=1
.ends

.GLOBAL VDD
.GLOBAL GND
.end
